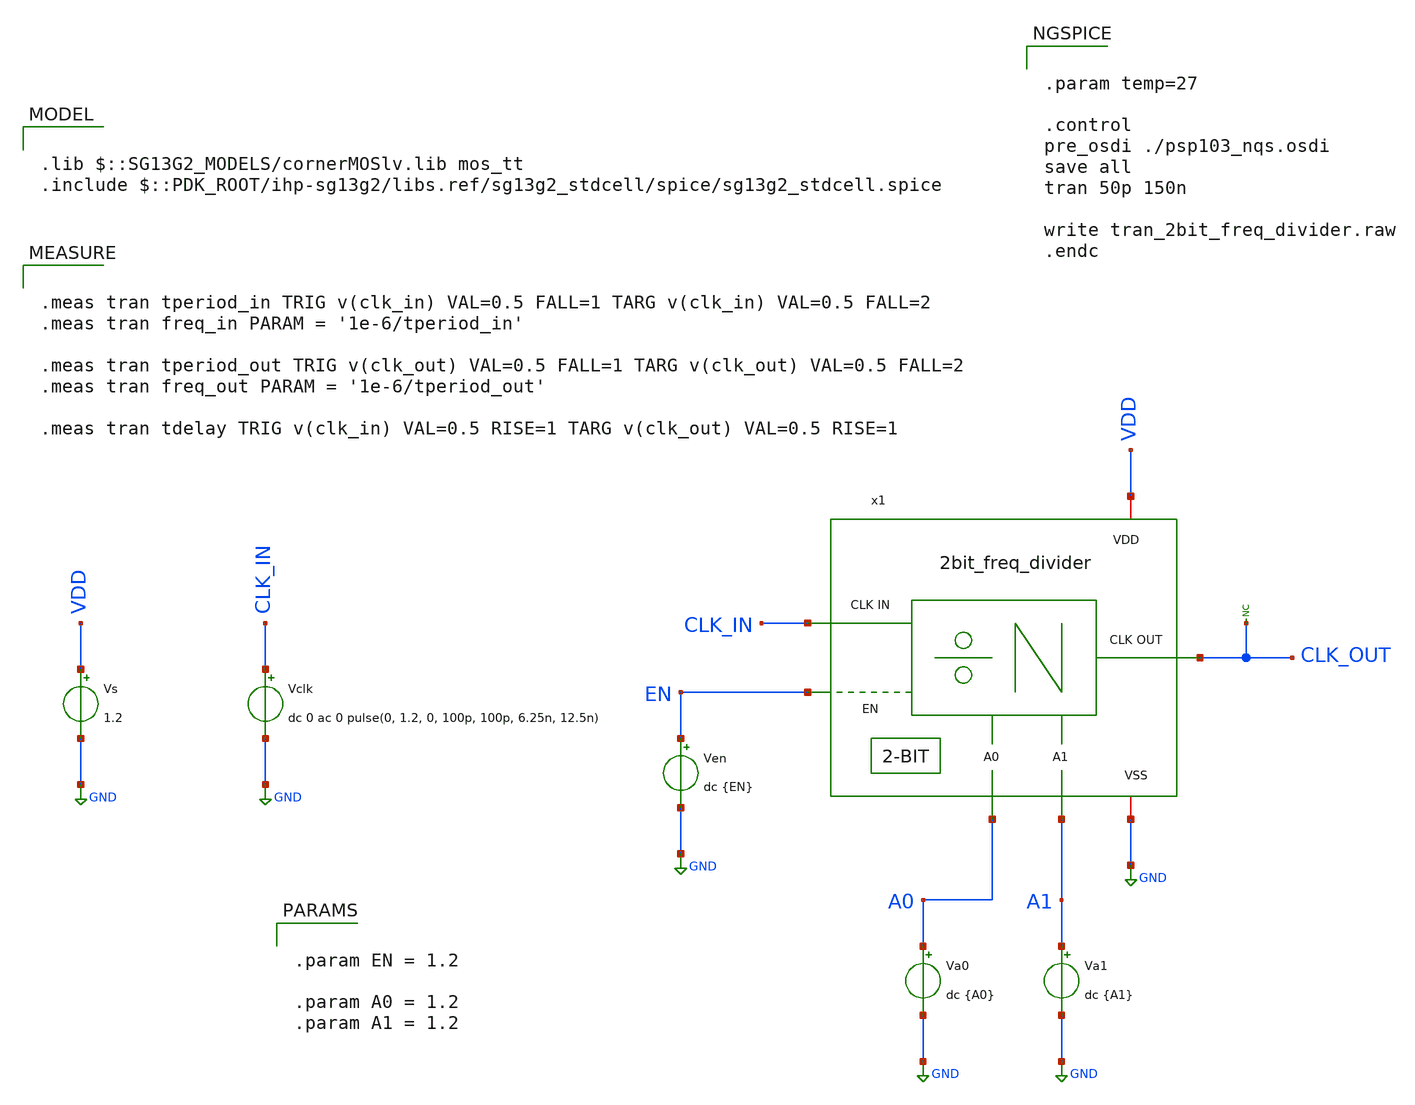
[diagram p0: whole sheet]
** sch_path: Combined Design/design_data/xschem/2bit_freq_divider_tb.sch

.lib $::SG13G2_MODELS/cornerMOSlv.lib mos_tt
.include $::PDK_ROOT/ihp-sg13g2/libs.ref/sg13g2_stdcell/spice/sg13g2_stdcell.spice

**.subckt 2bit_freq_divider_tb
Vs VDD GND 1.2
Vclk CLK_IN GND dc 0 ac 0 pulse(0, 1.2, 0, 100p, 100p, 6.25n, 12.5n)
* noconn CLK_OUT
Ven EN GND dc {EN}
Va0 A0 GND dc {A0}
Va1 A1 GND dc {A1}
x1 VDD GND A0 CLK_OUT CLK_IN EN A1 2bit_freq_divider
**** begin user architecture code


.meas tran tperiod_in TRIG v(clk_in) VAL=0.5 FALL=1 TARG v(clk_in) VAL=0.5 FALL=2
.meas tran freq_in PARAM = '1e-6/tperiod_in'

.meas tran tperiod_out TRIG v(clk_out) VAL=0.5 FALL=1 TARG v(clk_out) VAL=0.5 FALL=2
.meas tran freq_out PARAM = '1e-6/tperiod_out'

.meas tran tdelay TRIG v(clk_in) VAL=0.5 RISE=1 TARG v(clk_out) VAL=0.5 RISE=1




.param EN = 1.2

.param A0 = 1.2
.param A1 = 1.2




.param temp=27

.control
pre_osdi ./psp103_nqs.osdi
save all
tran 50p 150n

write tran_2bit_freq_divider.raw
.endc


**** end user architecture code
**.ends

* expanding   symbol:  2bit_freq_divider.sym # of pins=7
** sym_path: Combined Design/design_data/xschem/2bit_freq_divider.sym
** sch_path: Combined Design/design_data/xschem/2bit_freq_divider.sch
.subckt 2bit_freq_divider VDD VSS A0 CLK_OUT CLK_IN EN A1
*.ipin CLK_IN
*.ipin EN
*.ipin A0
*.ipin A1
*.opin CLK_OUT
*.iopin VSS
*.iopin VDD
x1 VDD VSS nEQ0 net1 CLK net2 DIV_RST A0 freq_div_cell
x2 VDD VSS nEQ1 net2 CLK Cout DIV_RST A1 freq_div_cell
x3 net5 VDD VSS sg13g2_tiehi
* noconn Cout
x4 DIV_RST nEQ0 nEQ1 VDD VSS sg13g2_or2_1
x5 DIV_RST CLK_OUT net3 net3 net4 VDD VSS dff_nclk
x6 net6 VDD VSS sg13g2_tiehi
* noconn CLK_OUT
x7 CLK CLK_IN EN VDD VSS sg13g2_nand2_1
.ends


* expanding   symbol:  sg13g2_stdcells/sg13g2_or2_1.sym # of pins=3
** sym_path: sg13g2_stdcells/sg13g2_or2_1.sym
** sch_path: sg13g2_stdcells/sg13g2_or2_1.sch
.subckt sg13g2_or2_1 X A B VDD VSS
*.opin X
*.ipin B
*.ipin A
*.iopin VDD
*.iopin VSS
XM1 net1 B VSS VSS sg13_lv_nmos w=550.00n l=130.00n ng=1 m=1 mm_ok=1
XM2 net1 A VSS VSS sg13_lv_nmos w=550.00n l=130.00n ng=1 m=1 mm_ok=1
XM3 X net1 VSS VSS sg13_lv_nmos w=740.00n l=130.00n ng=1 m=1 mm_ok=1
XM4 net2 A VDD VDD sg13_lv_pmos w=840.00n l=130.00n ng=1 m=1 mm_ok=1
XM5 net1 B net2 VDD sg13_lv_pmos w=840.00n l=130.00n ng=1 m=1 mm_ok=1
XM6 X net1 VDD VDD sg13_lv_pmos w=1.12u l=130.00n ng=1 m=1 mm_ok=1
.ends


* expanding   symbol:  sg13g2_stdcells/sg13g2_nand2_1.sym # of pins=3
** sym_path: sg13g2_stdcells/sg13g2_nand2_1.sym
** sch_path: sg13g2_stdcells/sg13g2_nand2_1.sch
.subckt sg13g2_nand2_1 Y A B VDD VSS
*.iopin VDD
*.iopin VSS
*.ipin A
*.ipin B
*.opin Y
XM1 Y A net1 VSS sg13_lv_nmos w=740.00n l=130.00n ng=1 m=1 mm_ok=1
XM2 net1 B VSS VSS sg13_lv_nmos w=740.00n l=130.00n ng=1 m=1 mm_ok=1
XM3 Y A VDD VDD sg13_lv_pmos w=1.12u l=130.00n ng=1 m=1 mm_ok=1
XM4 Y B VDD VDD sg13_lv_pmos w=1.12u l=130.00n ng=1 m=1 mm_ok=1
.ends

.GLOBAL GND
.end
